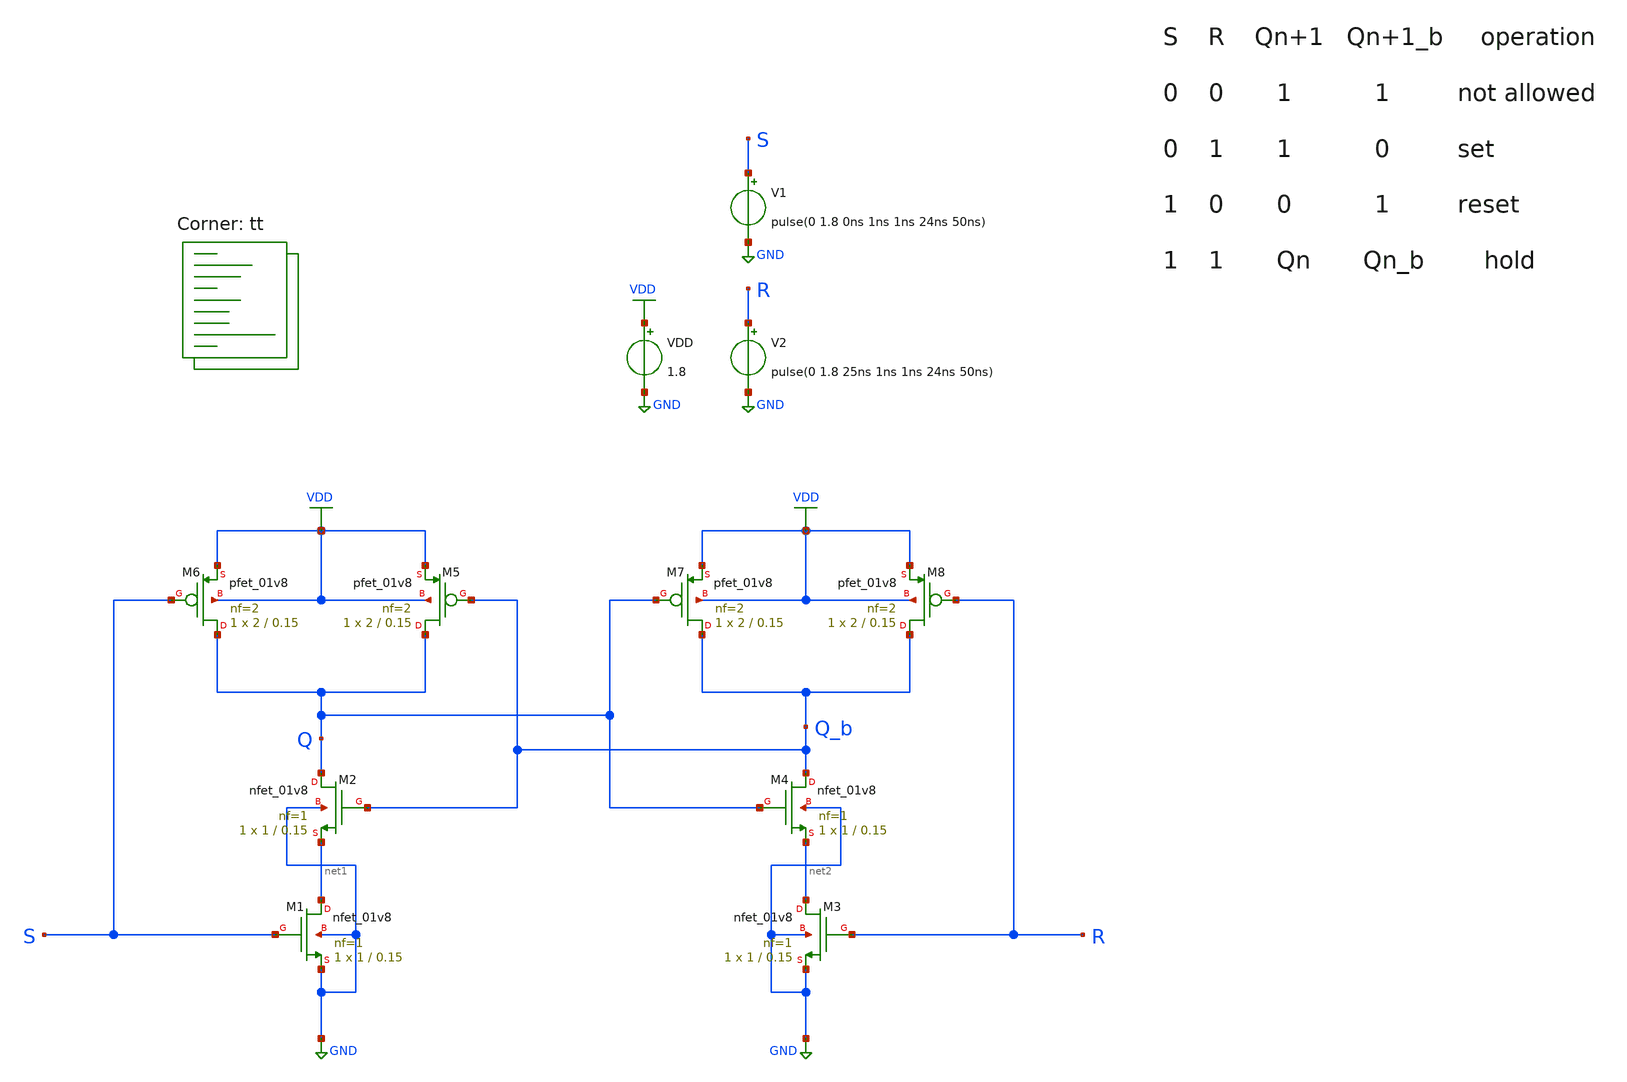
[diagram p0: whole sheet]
** sch_path: projects/pll/divider/xschem_ngspice/sr_latch_nand2.sch
**.subckt sr_latch_nand2
VDD VDD GND 1.8
V1 S GND pulse(0 1.8 0ns 1ns 1ns 24ns 50ns)
V2 R GND pulse(0 1.8 25ns 1ns 1ns 24ns 50ns)
XM1 net1 S GND GND sky130_fd_pr__nfet_01v8 L=0.15 W=1 nf=1 ad='int((nf+1)/2) * W/nf * 0.29' as='int((nf+2)/2) * W/nf * 0.29'
+ pd='2*int((nf+1)/2) * (W/nf + 0.29)' ps='2*int((nf+2)/2) * (W/nf + 0.29)' nrd='0.29 / W' nrs='0.29 / W'
+ sa=0 sb=0 sd=0 mult=1 m=1
XM2 Q Q_b net1 GND sky130_fd_pr__nfet_01v8 L=0.15 W=1 nf=1 ad='int((nf+1)/2) * W/nf * 0.29' as='int((nf+2)/2) * W/nf * 0.29'
+ pd='2*int((nf+1)/2) * (W/nf + 0.29)' ps='2*int((nf+2)/2) * (W/nf + 0.29)' nrd='0.29 / W' nrs='0.29 / W'
+ sa=0 sb=0 sd=0 mult=1 m=1
XM5 Q Q_b VDD VDD sky130_fd_pr__pfet_01v8 L=0.15 W=2 nf=2 ad='int((nf+1)/2) * W/nf * 0.29' as='int((nf+2)/2) * W/nf * 0.29'
+ pd='2*int((nf+1)/2) * (W/nf + 0.29)' ps='2*int((nf+2)/2) * (W/nf + 0.29)' nrd='0.29 / W' nrs='0.29 / W'
+ sa=0 sb=0 sd=0 mult=1 m=1
XM6 Q S VDD VDD sky130_fd_pr__pfet_01v8 L=0.15 W=2 nf=2 ad='int((nf+1)/2) * W/nf * 0.29' as='int((nf+2)/2) * W/nf * 0.29'
+ pd='2*int((nf+1)/2) * (W/nf + 0.29)' ps='2*int((nf+2)/2) * (W/nf + 0.29)' nrd='0.29 / W' nrs='0.29 / W'
+ sa=0 sb=0 sd=0 mult=1 m=1
XM3 net2 R GND GND sky130_fd_pr__nfet_01v8 L=0.15 W=1 nf=1 ad='int((nf+1)/2) * W/nf * 0.29' as='int((nf+2)/2) * W/nf * 0.29'
+ pd='2*int((nf+1)/2) * (W/nf + 0.29)' ps='2*int((nf+2)/2) * (W/nf + 0.29)' nrd='0.29 / W' nrs='0.29 / W'
+ sa=0 sb=0 sd=0 mult=1 m=1
XM4 Q_b Q net2 GND sky130_fd_pr__nfet_01v8 L=0.15 W=1 nf=1 ad='int((nf+1)/2) * W/nf * 0.29' as='int((nf+2)/2) * W/nf * 0.29'
+ pd='2*int((nf+1)/2) * (W/nf + 0.29)' ps='2*int((nf+2)/2) * (W/nf + 0.29)' nrd='0.29 / W' nrs='0.29 / W'
+ sa=0 sb=0 sd=0 mult=1 m=1
XM7 Q_b Q VDD VDD sky130_fd_pr__pfet_01v8 L=0.15 W=2 nf=2 ad='int((nf+1)/2) * W/nf * 0.29' as='int((nf+2)/2) * W/nf * 0.29'
+ pd='2*int((nf+1)/2) * (W/nf + 0.29)' ps='2*int((nf+2)/2) * (W/nf + 0.29)' nrd='0.29 / W' nrs='0.29 / W'
+ sa=0 sb=0 sd=0 mult=1 m=1
XM8 Q_b R VDD VDD sky130_fd_pr__pfet_01v8 L=0.15 W=2 nf=2 ad='int((nf+1)/2) * W/nf * 0.29' as='int((nf+2)/2) * W/nf * 0.29'
+ pd='2*int((nf+1)/2) * (W/nf + 0.29)' ps='2*int((nf+2)/2) * (W/nf + 0.29)' nrd='0.29 / W' nrs='0.29 / W'
+ sa=0 sb=0 sd=0 mult=1 m=1
**** begin user architecture code



.option method=gear
.option wnflag=1
.option savecurrents

.save @m.xm1.msky130_fd_pr__nfet_01v8[gm] @m.xm2.msky130_fd_pr__nfet_01v8[gm] @m.xm3.msky130_fd_pr__nfet_01v8[gm] @m.xm4.msky130_fd_pr__nfet_01v8[gm] @m.xm5.msky130_fd_pr__pfet_01v8[gm] @m.xm6.msky130_fd_pr__pfet_01v8[gm] @m.xm7.msky130_fd_pr__pfet_01v8[gm] @m.xm8.msky130_fd_pr__pfet_01v8[gm]


.control

  save v(s) v(r) v(q) v(q_b) v(ck)
  tran 0.1n 1u
  *ac dec 20 1 1T
  remzerovec
  write sr_ff_nand2.raw
  set appendwrite

.endc



.lib $::SKYWATER_MODELS/sky130.lib.spice tt
**** end user architecture code
**.ends
.GLOBAL GND
.GLOBAL VDD
.end
